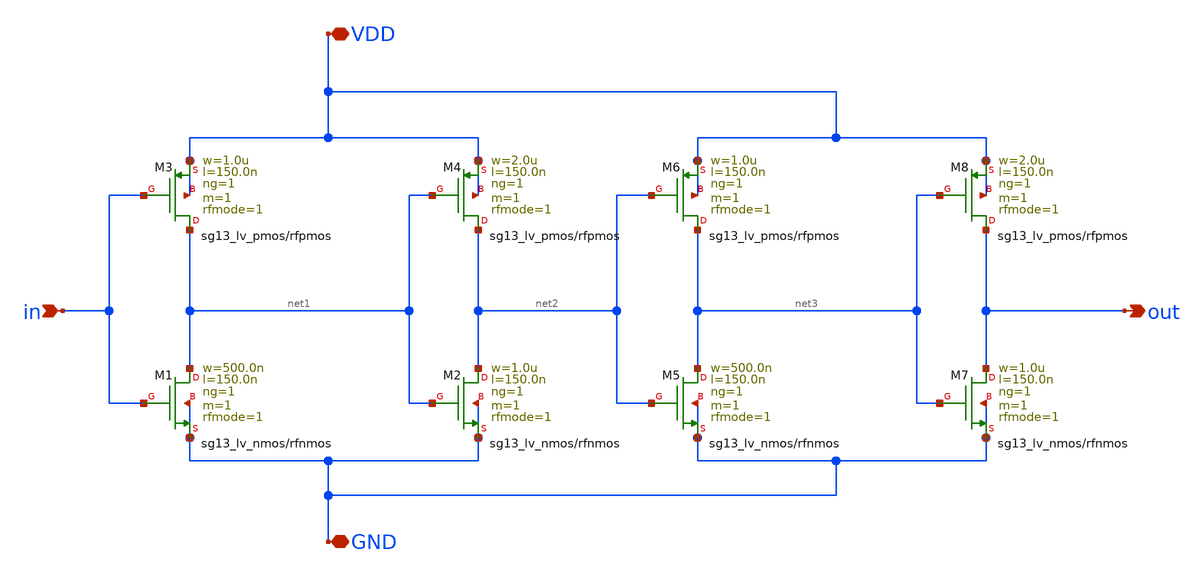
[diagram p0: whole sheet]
** sch_path: UWBPulseGenerator/design_data/xschem/buffer_inter.sch
**.subckt buffer_inter in out VDD GND
*.ipin in
*.opin out
*.iopin VDD
*.iopin GND
XM1 net1 in GND GND sg13_lv_nmos w=500.0n l=150.0n ng=1 m=1 rfmode=1 mm_ok=1
XM3 net1 in VDD VDD sg13_lv_pmos w=1.0u l=150.0n ng=1 m=1 rfmode=1 mm_ok=1
XM2 net2 net1 GND GND sg13_lv_nmos w=1.0u l=150.0n ng=1 m=1 rfmode=1 mm_ok=1
XM4 net2 net1 VDD VDD sg13_lv_pmos w=2.0u l=150.0n ng=1 m=1 rfmode=1 mm_ok=1
XM5 net3 net2 GND GND sg13_lv_nmos w=500.0n l=150.0n ng=1 m=1 rfmode=1 mm_ok=1
XM6 net3 net2 VDD VDD sg13_lv_pmos w=1.0u l=150.0n ng=1 m=1 rfmode=1 mm_ok=1
XM7 out net3 GND GND sg13_lv_nmos w=1.0u l=150.0n ng=1 m=1 rfmode=1 mm_ok=1
XM8 out net3 VDD VDD sg13_lv_pmos w=2.0u l=150.0n ng=1 m=1 rfmode=1 mm_ok=1
**.ends
.end
